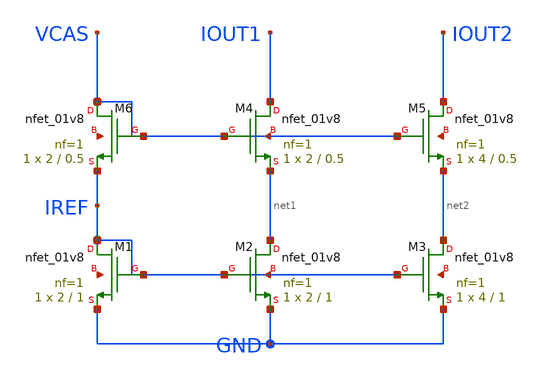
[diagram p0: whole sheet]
** sch_path: poc-strip-design/schematics/current_mirror.sch
**.subckt current_mirror
XM1 IREF IREF GND net3 sky130_fd_pr__nfet_01v8 L=1 W=2 nf=1 ad='int((1 + 1)/2) * 2 / 1 * 0.29' as='int((1 + 2)/2) * 2 / 1 * 0.29'
+ pd='2*int((1 + 1)/2) * (2 / 1 + 0.29)' ps='2*int((1 + 2)/2) * (2 / 1 + 0.29)' nrd='0.29 / 2 ' nrs='0.29 / 2 '
+ sa=0 sb=0 sd=0 mult=1 m=1
XM2 net1 IREF GND IREF sky130_fd_pr__nfet_01v8 L=1 W=2 nf=1 ad='int((1 + 1)/2) * 2 / 1 * 0.29' as='int((1 + 2)/2) * 2 / 1 * 0.29'
+ pd='2*int((1 + 1)/2) * (2 / 1 + 0.29)' ps='2*int((1 + 2)/2) * (2 / 1 + 0.29)' nrd='0.29 / 2 ' nrs='0.29 / 2 '
+ sa=0 sb=0 sd=0 mult=1 m=1
XM3 net2 IREF GND net4 sky130_fd_pr__nfet_01v8 L=1 W=4 nf=1 ad='int((1 + 1)/2) * 4 / 1 * 0.29' as='int((1 + 2)/2) * 4 / 1 * 0.29'
+ pd='2*int((1 + 1)/2) * (4 / 1 + 0.29)' ps='2*int((1 + 2)/2) * (4 / 1 + 0.29)' nrd='0.29 / 4 ' nrs='0.29 / 4 '
+ sa=0 sb=0 sd=0 mult=1 m=1
XM6 VCAS VCAS IREF net5 sky130_fd_pr__nfet_01v8 L=0.5 W=2 nf=1 ad='int((1 + 1)/2) * 2 / 1 * 0.29' as='int((1 + 2)/2) * 2 / 1 * 0.29'
+ pd='2*int((1 + 1)/2) * (2 / 1 + 0.29)' ps='2*int((1 + 2)/2) * (2 / 1 + 0.29)' nrd='0.29 / 2 ' nrs='0.29 / 2 '
+ sa=0 sb=0 sd=0 mult=1 m=1
XM4 IOUT1 VCAS net1 VCAS sky130_fd_pr__nfet_01v8 L=0.5 W=2 nf=1 ad='int((1 + 1)/2) * 2 / 1 * 0.29' as='int((1 + 2)/2) * 2 / 1 * 0.29'
+ pd='2*int((1 + 1)/2) * (2 / 1 + 0.29)' ps='2*int((1 + 2)/2) * (2 / 1 + 0.29)' nrd='0.29 / 2 ' nrs='0.29 / 2 '
+ sa=0 sb=0 sd=0 mult=1 m=1
XM5 IOUT2 VCAS net2 net6 sky130_fd_pr__nfet_01v8 L=0.5 W=4 nf=1 ad='int((1 + 1)/2) * 4 / 1 * 0.29' as='int((1 + 2)/2) * 4 / 1 * 0.29'
+ pd='2*int((1 + 1)/2) * (4 / 1 + 0.29)' ps='2*int((1 + 2)/2) * (4 / 1 + 0.29)' nrd='0.29 / 4 ' nrs='0.29 / 4 '
+ sa=0 sb=0 sd=0 mult=1 m=1
**.ends
.end
